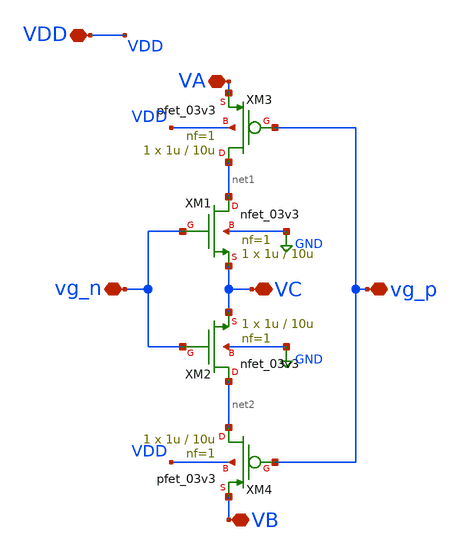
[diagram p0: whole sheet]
** sch_path: TIA/xschem/pseudo_res_dir/PR_single.sch
**.subckt PR_single VB VA vg_n vg_p VC VDD
*.iopin VB
*.iopin VA
*.iopin vg_n
*.iopin vg_p
*.iopin VC
*.iopin VDD
XM1 net1 vg_n VC GND nfet_03v3 L=10u W=1u nf=1 ad='int((nf+1)/2) * W/nf * 0.18u' as='int((nf+2)/2) * W/nf * 0.18u'
+ pd='2*int((nf+1)/2) * (W/nf + 0.18u)' ps='2*int((nf+2)/2) * (W/nf + 0.18u)' nrd='0.18u / W' nrs='0.18u / W'
+ sa=0 sb=0 sd=0 m=1
XM3 net1 vg_p VA VDD pfet_03v3 L=10u W=1u nf=1 ad='int((nf+1)/2) * W/nf * 0.18u' as='int((nf+2)/2) * W/nf * 0.18u'
+ pd='2*int((nf+1)/2) * (W/nf + 0.18u)' ps='2*int((nf+2)/2) * (W/nf + 0.18u)' nrd='0.18u / W' nrs='0.18u / W'
+ sa=0 sb=0 sd=0 m=1
XM2 net2 vg_n VC GND nfet_03v3 L=10u W=1u nf=1 ad='int((nf+1)/2) * W/nf * 0.18u' as='int((nf+2)/2) * W/nf * 0.18u'
+ pd='2*int((nf+1)/2) * (W/nf + 0.18u)' ps='2*int((nf+2)/2) * (W/nf + 0.18u)' nrd='0.18u / W' nrs='0.18u / W'
+ sa=0 sb=0 sd=0 m=1
XM4 net2 vg_p VB VDD pfet_03v3 L=10u W=1u nf=1 ad='int((nf+1)/2) * W/nf * 0.18u' as='int((nf+2)/2) * W/nf * 0.18u'
+ pd='2*int((nf+1)/2) * (W/nf + 0.18u)' ps='2*int((nf+2)/2) * (W/nf + 0.18u)' nrd='0.18u / W' nrs='0.18u / W'
+ sa=0 sb=0 sd=0 m=1
**.ends
.GLOBAL GND
.end
